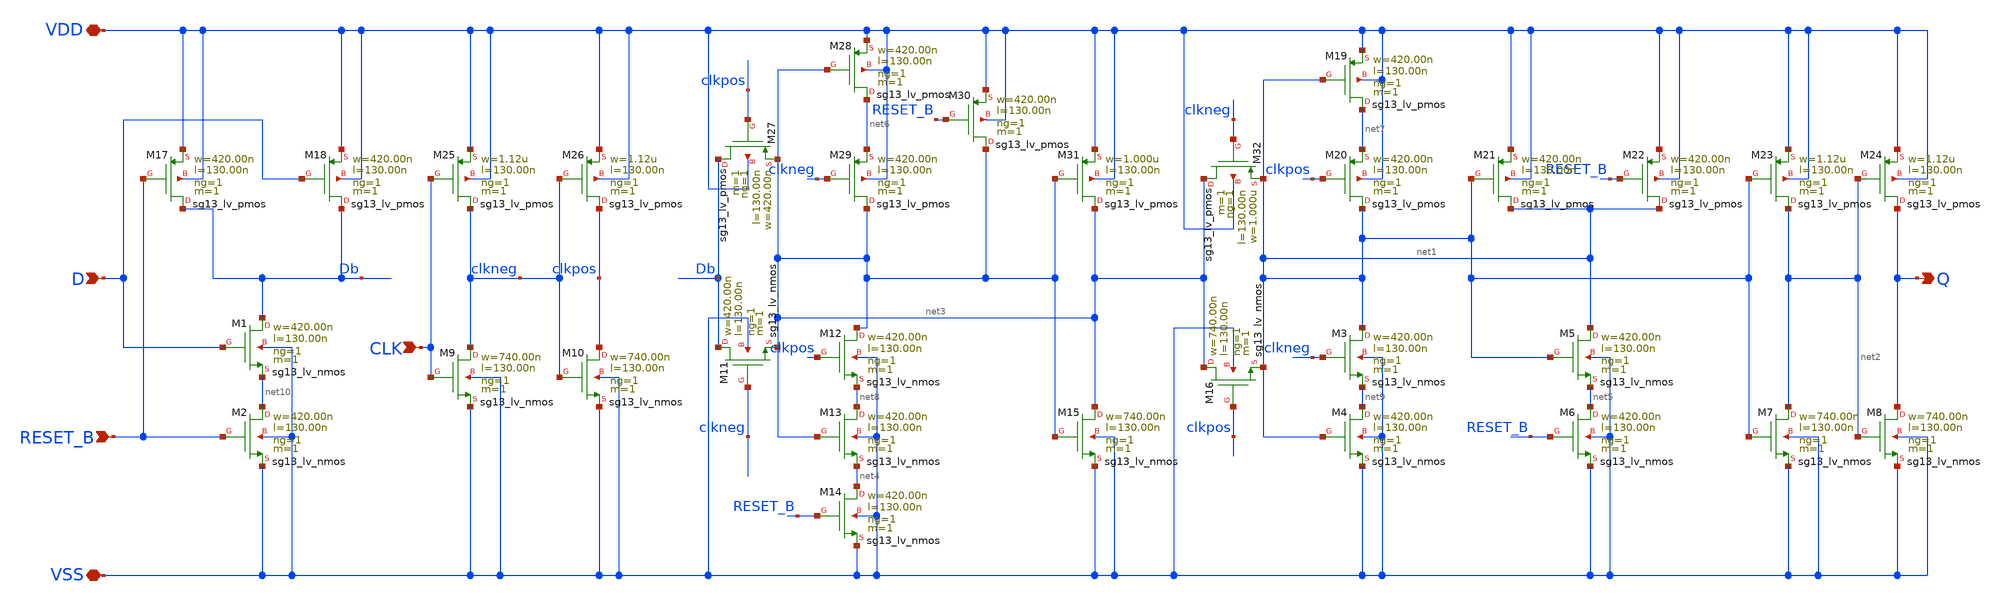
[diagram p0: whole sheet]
** sch_path: ihp-sg13g2/libs.tech/xschem/sg13g2_stdcells/sg13g2_dfrbpq_1.sch
* Copyright 2023 IHP PDK Authors
* Licensed under the Apache License, Version 2.0 (the "License");
* you may not use this file except in compliance with the License.
* You may obtain a copy of the License at
* https://www.apache.org/licenses/LICENSE-2.0
* Unless required by applicable law or agreed to in writing, software
* distributed under the License is distributed on an "AS IS" BASIS,
* WITHOUT WARRANTIES OR CONDITIONS OF ANY KIND, either express or implied.
* See the License for the specific language governing permissions and
* limitations under the License.
**.subckt sg13g2_dfrbpq_1 Q CLK D RESET_B VDD VSS
*.opin Q
*.ipin CLK
*.ipin D
*.ipin RESET_B
*.iopin VDD
*.iopin VSS
XM1 Db D net10 VSS sg13_lv_nmos w=420.00n l=130.00n ng=1 m=1 mm_ok=1
XM2 net10 RESET_B VSS VSS sg13_lv_nmos w=420.00n l=130.00n ng=1 m=1 mm_ok=1
XM3 net1 clkneg net9 VSS sg13_lv_nmos w=420.00n l=130.00n ng=1 m=1 mm_ok=1
XM4 net9 net1 VSS VSS sg13_lv_nmos w=420.00n l=130.00n ng=1 m=1 mm_ok=1
XM5 net1 net1 net5 VSS sg13_lv_nmos w=420.00n l=130.00n ng=1 m=1 mm_ok=1
XM6 net5 RESET_B VSS VSS sg13_lv_nmos w=420.00n l=130.00n ng=1 m=1 mm_ok=1
XM7 net2 net1 VSS VSS sg13_lv_nmos w=740.00n l=130.00n ng=1 m=1 mm_ok=1
XM8 Q net2 VSS VSS sg13_lv_nmos w=740.00n l=130.00n ng=1 m=1 mm_ok=1
XM9 clkneg CLK VSS VSS sg13_lv_nmos w=740.00n l=130.00n ng=1 m=1 mm_ok=1
XM10 clkpos clkneg VSS VSS sg13_lv_nmos w=740.00n l=130.00n ng=1 m=1 mm_ok=1
XM11 Db clkneg net3 VSS sg13_lv_nmos w=420.00n l=130.00n ng=1 m=1 mm_ok=1
XM12 net3 clkpos net8 VSS sg13_lv_nmos w=420.00n l=130.00n ng=1 m=1 mm_ok=1
XM13 net8 net3 net4 VSS sg13_lv_nmos w=420.00n l=130.00n ng=1 m=1 mm_ok=1
XM14 net4 RESET_B VSS VSS sg13_lv_nmos w=420.00n l=130.00n ng=1 m=1 mm_ok=1
XM15 net3 net3 VSS VSS sg13_lv_nmos w=740.00n l=130.00n ng=1 m=1 mm_ok=1
XM16 net3 clkpos net1 VSS sg13_lv_nmos w=740.00n l=130.00n ng=1 m=1 mm_ok=1
XM17 Db RESET_B VDD VDD sg13_lv_pmos w=420.00n l=130.00n ng=1 m=1 mm_ok=1
XM18 Db D VDD VDD sg13_lv_pmos w=420.00n l=130.00n ng=1 m=1 mm_ok=1
XM19 net7 net1 VDD VDD sg13_lv_pmos w=420.00n l=130.00n ng=1 m=1 mm_ok=1
XM20 net1 clkpos net7 VDD sg13_lv_pmos w=420.00n l=130.00n ng=1 m=1 mm_ok=1
XM21 net1 net1 VDD VDD sg13_lv_pmos w=420.00n l=130.00n ng=1 m=1 mm_ok=1
XM22 net1 RESET_B VDD VDD sg13_lv_pmos w=420.00n l=130.00n ng=1 m=1 mm_ok=1
XM23 net2 net1 VDD VDD sg13_lv_pmos w=1.12u l=130.00n ng=1 m=1 mm_ok=1
XM24 Q net2 VDD VDD sg13_lv_pmos w=1.12u l=130.00n ng=1 m=1 mm_ok=1
XM25 clkneg CLK VDD VDD sg13_lv_pmos w=1.12u l=130.00n ng=1 m=1 mm_ok=1
XM26 clkpos clkneg VDD VDD sg13_lv_pmos w=1.12u l=130.00n ng=1 m=1 mm_ok=1
XM27 Db clkpos net3 VDD sg13_lv_pmos w=420.00n l=130.00n ng=1 m=1 mm_ok=1
XM28 net6 net3 VDD VDD sg13_lv_pmos w=420.00n l=130.00n ng=1 m=1 mm_ok=1
XM29 net3 clkneg net6 VDD sg13_lv_pmos w=420.00n l=130.00n ng=1 m=1 mm_ok=1
XM30 net3 RESET_B VDD VDD sg13_lv_pmos w=420.00n l=130.00n ng=1 m=1 mm_ok=1
XM31 net3 net3 VDD VDD sg13_lv_pmos w=1.000u l=130.00n ng=1 m=1 mm_ok=1
XM32 net3 clkneg net1 VDD sg13_lv_pmos w=1.000u l=130.00n ng=1 m=1 mm_ok=1
**.ends
.end
